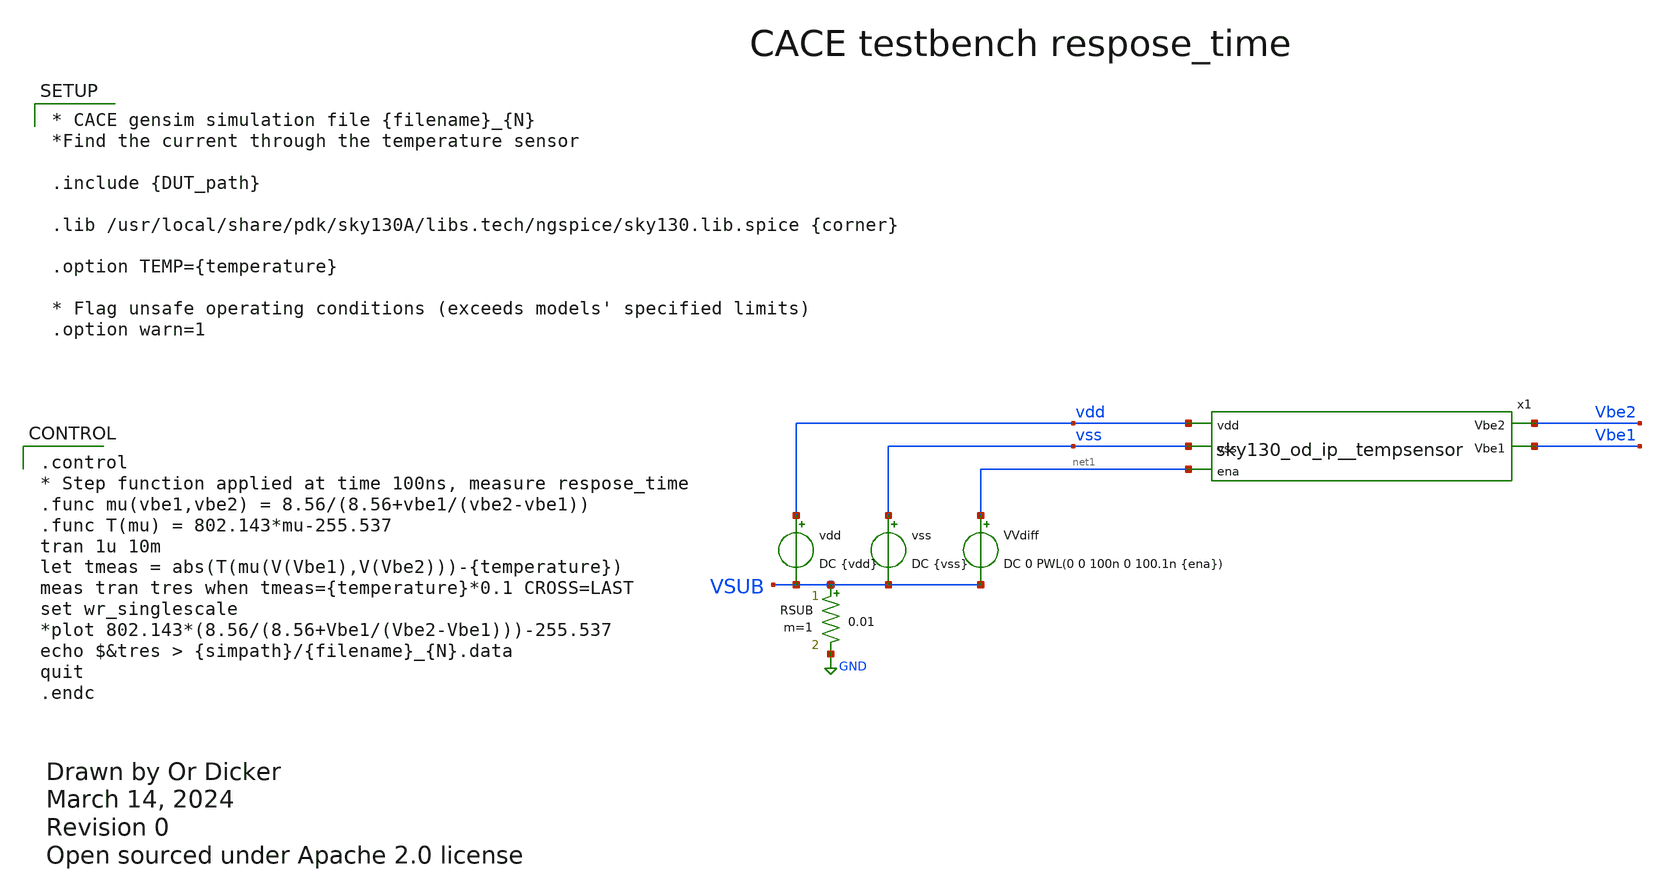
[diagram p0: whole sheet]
** sch_path: cace/respose_time.sch
* Open sourced under Apache 2.0 license
**.subckt respose_time
vss vss VSUB DC {vss}
vdd vdd VSUB DC {vdd}
RSUB VSUB GND 0.01 m=1
x1 vdd vss Vbe2 Vbe1 net1 sky130_od_ip__tempsensor
VVdiff net1 VSUB DC 0 PWL(0 0 100n 0 100.1n {ena})
**** begin user architecture code

.control
* Step function applied at time 100ns, measure respose_time
.func mu(vbe1,vbe2) = 8.56/(8.56+vbe1/(vbe2-vbe1))
.func T(mu) = 802.143*mu-255.537
tran 1u 10m
let tmeas = abs(T(mu(V(Vbe1),V(Vbe2)))-{temperature})
meas tran tres when tmeas={temperature}*0.1 CROSS=LAST
set wr_singlescale
*plot 802.143*(8.56/(8.56+Vbe1/(Vbe2-Vbe1)))-255.537
echo $&tres > {simpath}/{filename}_{N}.data
quit
.endc



* CACE gensim simulation file {filename}_{N}
*Find the current through the temperature sensor

.include {DUT_path}

.lib /usr/local/share/pdk/sky130A/libs.tech/ngspice/sky130.lib.spice {corner}

.option TEMP={temperature}

* Flag unsafe operating conditions (exceeds models' specified limits)
.option warn=1


**** end user architecture code
**.ends

* expanding   symbol:  xschem/sky130_od_ip__tempsensor.sym # of pins=5
** sym_path: xschem/sky130_od_ip__tempsensor.sym
** sch_path: xschem/sky130_od_ip__tempsensor.sch
.subckt sky130_od_ip__tempsensor vdd vss Vbe2 Vbe1 ena
*.ipin vdd
*.ipin vss
*.opin Vbe2
*.opin Vbe1
*.ipin ena
XM12 net1 Vp vdd vdd sky130_fd_pr__pfet_01v8 L=1.2 W=1 nf=1 ad='int((nf+1)/2) * W/nf * 0.29' as='int((nf+2)/2)
+ * W/nf * 0.29' pd='2*int((nf+1)/2) * (W/nf + 0.29)' ps='2*int((nf+2)/2) * (W/nf + 0.29)' nrd='0.29 /
+ W' nrs='0.29 / W' sa=0 sb=0 sd=0 mult=5 m=5
XM13 net2 Vp vdd vdd sky130_fd_pr__pfet_01v8 L=1.2 W=1 nf=1 ad='int((nf+1)/2) * W/nf * 0.29' as='int((nf+2)/2)
+ * W/nf * 0.29' pd='2*int((nf+1)/2) * (W/nf + 0.29)' ps='2*int((nf+2)/2) * (W/nf + 0.29)' nrd='0.29 /
+ W' nrs='0.29 / W' sa=0 sb=0 sd=0 mult=1 m=1
XQ_BR vss net3 net1 sky130_fd_pr__pnp_05v5_W3p40L3p40 m=1
XQ_BL vss vss net4 sky130_fd_pr__pnp_05v5_W3p40L3p40 m=1
Rb net2 net4 5k m=1
Rb_5 net3 vss 1k m=1
XM11 net5 Vp vdd vdd sky130_fd_pr__pfet_01v8 L=1.2 W=1 nf=1 ad='int((nf+1)/2) * W/nf * 0.29' as='int((nf+2)/2)
+ * W/nf * 0.29' pd='2*int((nf+1)/2) * (W/nf + 0.29)' ps='2*int((nf+2)/2) * (W/nf + 0.29)' nrd='0.29 /
+ W' nrs='0.29 / W' sa=0 sb=0 sd=0 mult=2 m=2
XM6 net6 net2 net5 net5 sky130_fd_pr__pfet_01v8 L=1.2 W=10 nf=1 ad='int((nf+1)/2) * W/nf * 0.29' as='int((nf+2)/2)
+ * W/nf * 0.29' pd='2*int((nf+1)/2) * (W/nf + 0.29)' ps='2*int((nf+2)/2) * (W/nf + 0.29)' nrd='0.29 /
+ W' nrs='0.29 / W' sa=0 sb=0 sd=0 mult=1 m=1
XM5 net7 net1 net5 net5 sky130_fd_pr__pfet_01v8 L=1.2 W=10 nf=1 ad='int((nf+1)/2) * W/nf * 0.29' as='int((nf+2)/2)
+ * W/nf * 0.29' pd='2*int((nf+1)/2) * (W/nf + 0.29)' ps='2*int((nf+2)/2) * (W/nf + 0.29)' nrd='0.29 /
+ W' nrs='0.29 / W' sa=0 sb=0 sd=0 mult=1 m=1
XM2 net6 net7 vss vss sky130_fd_pr__nfet_01v8 L=1.2 W=10 nf=1 ad='int((nf+1)/2) * W/nf * 0.29' as='int((nf+2)/2)
+ * W/nf * 0.29' pd='2*int((nf+1)/2) * (W/nf + 0.29)' ps='2*int((nf+2)/2) * (W/nf + 0.29)' nrd='0.29 /
+ W' nrs='0.29 / W' sa=0 sb=0 sd=0 mult=1 m=1
XM1 net7 net7 vss vss sky130_fd_pr__nfet_01v8 L=1.2 W=10 nf=1 ad='int((nf+1)/2) * W/nf * 0.29' as='int((nf+2)/2)
+ * W/nf * 0.29' pd='2*int((nf+1)/2) * (W/nf + 0.29)' ps='2*int((nf+2)/2) * (W/nf + 0.29)' nrd='0.29 /
+ W' nrs='0.29 / W' sa=0 sb=0 sd=0 mult=1 m=1
XM9 net8 Vp vdd vdd sky130_fd_pr__pfet_01v8 L=1.2 W=1 nf=1 ad='int((nf+1)/2) * W/nf * 0.29' as='int((nf+2)/2)
+ * W/nf * 0.29' pd='2*int((nf+1)/2) * (W/nf + 0.29)' ps='2*int((nf+2)/2) * (W/nf + 0.29)' nrd='0.29 /
+ W' nrs='0.29 / W' sa=0 sb=0 sd=0 mult=1 m=1
XM10 Vp Vp vdd vdd sky130_fd_pr__pfet_01v8 L=1.2 W=1 nf=1 ad='int((nf+1)/2) * W/nf * 0.29' as='int((nf+2)/2)
+ * W/nf * 0.29' pd='2*int((nf+1)/2) * (W/nf + 0.29)' ps='2*int((nf+2)/2) * (W/nf + 0.29)' nrd='0.29 /
+ W' nrs='0.29 / W' sa=0 sb=0 sd=0 mult=4 m=4
XM7 Vp net8 net10 net10 sky130_fd_pr__nfet_01v8 L=1.2 W=10 nf=1 ad='int((nf+1)/2) * W/nf * 0.29' as='int((nf+2)/2)
+ * W/nf * 0.29' pd='2*int((nf+1)/2) * (W/nf + 0.29)' ps='2*int((nf+2)/2) * (W/nf + 0.29)' nrd='0.29 /
+ W' nrs='0.29 / W' sa=0 sb=0 sd=0 mult=1 m=1
XM8 net8 net8 net9 net9 sky130_fd_pr__nfet_01v8 L=1.2 W=10 nf=1 ad='int((nf+1)/2) * W/nf * 0.29' as='int((nf+2)/2)
+ * W/nf * 0.29' pd='2*int((nf+1)/2) * (W/nf + 0.29)' ps='2*int((nf+2)/2) * (W/nf + 0.29)' nrd='0.29 /
+ W' nrs='0.29 / W' sa=0 sb=0 sd=0 mult=1 m=1
XM3 net10 net6 vss vss sky130_fd_pr__nfet_01v8 L=1.2 W=10 nf=1 ad='int((nf+1)/2) * W/nf * 0.29' as='int((nf+2)/2)
+ * W/nf * 0.29' pd='2*int((nf+1)/2) * (W/nf + 0.29)' ps='2*int((nf+2)/2) * (W/nf + 0.29)' nrd='0.29 /
+ W' nrs='0.29 / W' sa=0 sb=0 sd=0 mult=4 m=4
XM4 net9 net9 vss vss sky130_fd_pr__nfet_01v8 L=1.2 W=1 nf=1 ad='int((nf+1)/2) * W/nf * 0.29' as='int((nf+2)/2)
+ * W/nf * 0.29' pd='2*int((nf+1)/2) * (W/nf + 0.29)' ps='2*int((nf+2)/2) * (W/nf + 0.29)' nrd='0.29 /
+ W' nrs='0.29 / W' sa=0 sb=0 sd=0 mult=20 m=20
XQ_BL1 vss vss Vbe1 sky130_fd_pr__pnp_05v5_W3p40L3p40 m=1
XQ_BR1 vss vss Vbe2 sky130_fd_pr__pnp_05v5_W3p40L3p40 m=1
XM14 Vbe1 Vp vdd vdd sky130_fd_pr__pfet_01v8 L=1.2 W=1 nf=1 ad='int((nf+1)/2) * W/nf * 0.29' as='int((nf+2)/2)
+ * W/nf * 0.29' pd='2*int((nf+1)/2) * (W/nf + 0.29)' ps='2*int((nf+2)/2) * (W/nf + 0.29)' nrd='0.29 /
+ W' nrs='0.29 / W' sa=0 sb=0 sd=0 mult=1 m=1
XM15 Vbe2 Vp vdd vdd sky130_fd_pr__pfet_01v8 L=1.2 W=1 nf=1 ad='int((nf+1)/2) * W/nf * 0.29' as='int((nf+2)/2)
+ * W/nf * 0.29' pd='2*int((nf+1)/2) * (W/nf + 0.29)' ps='2*int((nf+2)/2) * (W/nf + 0.29)' nrd='0.29 /
+ W' nrs='0.29 / W' sa=0 sb=0 sd=0 mult=5 m=5
XM16 Vp ena vdd vdd sky130_fd_pr__pfet_01v8 L=1.2 W=10 nf=1 ad='int((nf+1)/2) * W/nf * 0.29' as='int((nf+2)/2)
+ * W/nf * 0.29' pd='2*int((nf+1)/2) * (W/nf + 0.29)' ps='2*int((nf+2)/2) * (W/nf + 0.29)' nrd='0.29 /
+ W' nrs='0.29 / W' sa=0 sb=0 sd=0 mult=1 m=1
.ends

.GLOBAL GND
.end
